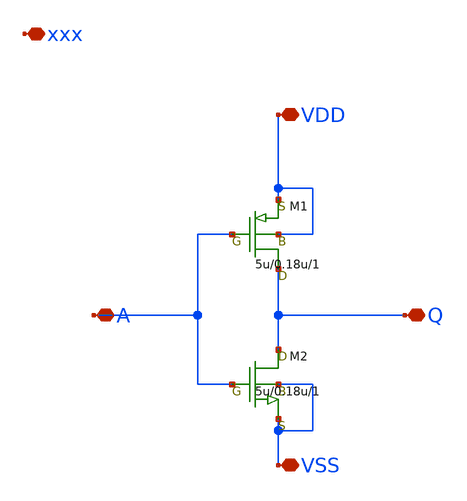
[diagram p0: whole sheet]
** sch_path: member_project/Hizuki1030/my-inverter-lsi/untitled.sch
**.subckt untitled xxx A Q VDD VSS
*.iopin xxx
*.iopin A
*.iopin Q
*.iopin VDD
*.iopin VSS
M1 Q A VDD VDD pch w=5u l=0.18u as=0 ps=0 ad=0 pd=0 m=1
M2 Q A VSS VSS nch w=5u l=0.18u as=0 ps=0 ad=0 pd=0 m=1
**.ends
.end
